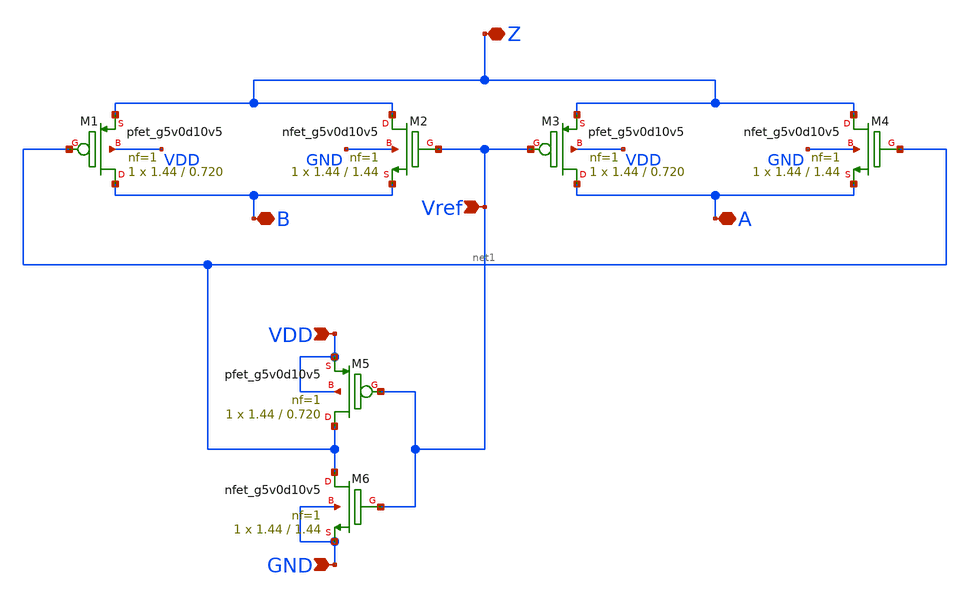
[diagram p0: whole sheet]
** sch_path: xschem/schematic_lvs/switch.sch
**.subckt switch Vref Z A B VDD GND
*.ipin Vref
*.iopin Z
*.iopin A
*.iopin B
*.ipin VDD
*.ipin GND
XM2 Z Vref B GND sky130_fd_pr__nfet_g5v0d10v5 L=1.44 W=1.44 nf=1 ad='int((1 + 1)/2) * 1.44 / 1 * 0.29'
+ as='int((1 + 2)/2) * 1.44 / 1 * 0.29' pd='2*int((1 + 1)/2) * (1.44 / 1 + 0.29)' ps='2*int((1 + 2)/2) * (1.44 / 1 + 0.29)'
+ nrd='0.29 / 1.44 ' nrs='0.29 / 1.44 ' sa=0 sb=0 sd=0 mult=1 m=1
XM1 B net1 Z VDD sky130_fd_pr__pfet_g5v0d10v5 L=0.720 W=1.44 nf=1 ad='int((1 + 1)/2) * 1.44 / 1 * 0.29'
+ as='int((1 + 2)/2) * 1.44 / 1 * 0.29' pd='2*int((1 + 1)/2) * (1.44 / 1 + 0.29)' ps='2*int((1 + 2)/2) * (1.44 / 1 + 0.29)'
+ nrd='0.29 / 1.44 ' nrs='0.29 / 1.44 ' sa=0 sb=0 sd=0 mult=1 m=1
XM3 A Vref Z VDD sky130_fd_pr__pfet_g5v0d10v5 L=0.720 W=1.44 nf=1 ad='int((1 + 1)/2) * 1.44 / 1 * 0.29'
+ as='int((1 + 2)/2) * 1.44 / 1 * 0.29' pd='2*int((1 + 1)/2) * (1.44 / 1 + 0.29)' ps='2*int((1 + 2)/2) * (1.44 / 1 + 0.29)'
+ nrd='0.29 / 1.44 ' nrs='0.29 / 1.44 ' sa=0 sb=0 sd=0 mult=1 m=1
XM5 net1 Vref VDD VDD sky130_fd_pr__pfet_g5v0d10v5 L=0.720 W=1.44 nf=1 ad='int((1 + 1)/2) * 1.44 / 1 * 0.29'
+ as='int((1 + 2)/2) * 1.44 / 1 * 0.29' pd='2*int((1 + 1)/2) * (1.44 / 1 + 0.29)' ps='2*int((1 + 2)/2) * (1.44 / 1 + 0.29)'
+ nrd='0.29 / 1.44 ' nrs='0.29 / 1.44 ' sa=0 sb=0 sd=0 mult=1 m=1
XM4 Z net1 A GND sky130_fd_pr__nfet_g5v0d10v5 L=1.44 W=1.44 nf=1 ad='int((1 + 1)/2) * 1.44 / 1 * 0.29'
+ as='int((1 + 2)/2) * 1.44 / 1 * 0.29' pd='2*int((1 + 1)/2) * (1.44 / 1 + 0.29)' ps='2*int((1 + 2)/2) * (1.44 / 1 + 0.29)'
+ nrd='0.29 / 1.44 ' nrs='0.29 / 1.44 ' sa=0 sb=0 sd=0 mult=1 m=1
XM6 net1 Vref GND GND sky130_fd_pr__nfet_g5v0d10v5 L=1.44 W=1.44 nf=1 ad='int((1 + 1)/2) * 1.44 / 1 * 0.29'
+ as='int((1 + 2)/2) * 1.44 / 1 * 0.29' pd='2*int((1 + 1)/2) * (1.44 / 1 + 0.29)' ps='2*int((1 + 2)/2) * (1.44 / 1 + 0.29)'
+ nrd='0.29 / 1.44 ' nrs='0.29 / 1.44 ' sa=0 sb=0 sd=0 mult=1 m=1
**.ends
.end
